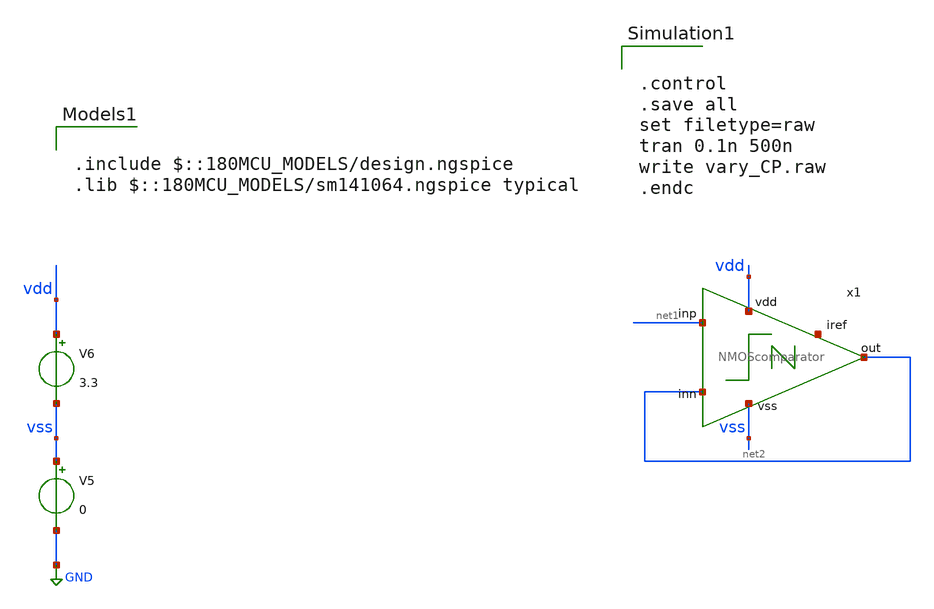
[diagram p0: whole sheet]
** sch_path: designs/libs/qw_core_analog/otatest.sch
**.subckt otatest
x1 vdd net1 net2 net2 net3 vss NMOScomparator
V5 vss GND 0
V6 vdd vss 3.3
**** begin user architecture code

.include $::180MCU_MODELS/design.ngspice
.lib $::180MCU_MODELS/sm141064.ngspice typical



.control
.save all
set filetype=raw
tran 0.1n 500n
write vary_CP.raw
.endc


**** end user architecture code
**.ends
.GLOBAL GND
.end
